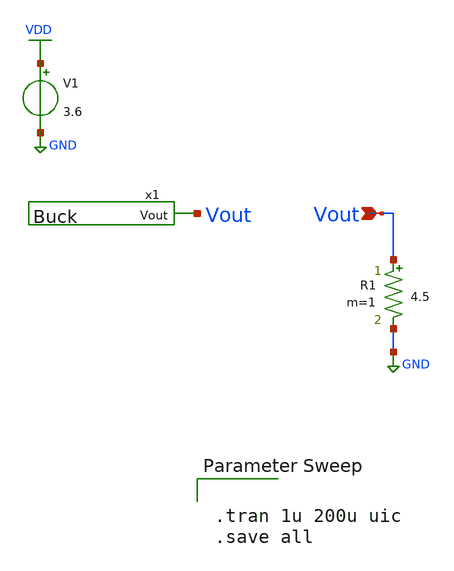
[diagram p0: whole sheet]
** sch_path: Ene_Thompson/test_Buck.sch
**.subckt test_Buck Vout
*.ipin Vout
x1 Vout Buck
V1 VDD GND 3.6
R1 Vout GND 4.5 m=1
**** begin user architecture code

.lib $::SKYWATER_MODELS/sky130.lib.spice tt



.tran 1u 200u uic
.save all


**** end user architecture code
**.ends

* expanding   symbol:  Buck.sym # of pins=1
** sym_path: Ene_Thompson/Buck.sym
** sch_path: Ene_Thompson/Buck.sch
.subckt Buck Vout
*.opin Vout
XM1 vl pswitch net1 VDD sky130_fd_pr__pfet_g5v0d10v5 L=0.5 W=20 nf=1 ad='int((nf+1)/2) * W/nf * 0.29'
+ as='int((nf+2)/2) * W/nf * 0.29' pd='2*int((nf+1)/2) * (W/nf + 0.29)' ps='2*int((nf+2)/2) * (W/nf + 0.29)'
+ nrd='0.29 / W' nrs='0.29 / W' sa=0 sb=0 sd=0 mult=1333 m=1333
XM2 vl nswitch net4 GND sky130_fd_pr__nfet_g5v0d10v5 L=0.5 W=20 nf=1 ad='int((nf+1)/2) * W/nf * 0.29'
+ as='int((nf+2)/2) * W/nf * 0.29' pd='2*int((nf+1)/2) * (W/nf + 0.29)' ps='2*int((nf+2)/2) * (W/nf + 0.29)'
+ nrd='0.29 / W' nrs='0.29 / W' sa=0 sb=0 sd=0 mult=667 m=667
L1 net3 Vout 4.7u m=1
C1 Vout net2 1u m=1
V1 pswitch GND PULSE(0 5 0 0.01u 0.01u 0.5u 1u)
R1 vl net3 1.5m m=1
R2 GND net2 10m m=1
V2 nswitch GND PULSE(0 5 75n 0.01u 0.01u 0.35u 1u)
Vm1 VDD net1 0
.save i(vm1)
Vm2 net4 GND 0
.save i(vm2)
.ends

.GLOBAL VDD
.GLOBAL GND
.end
